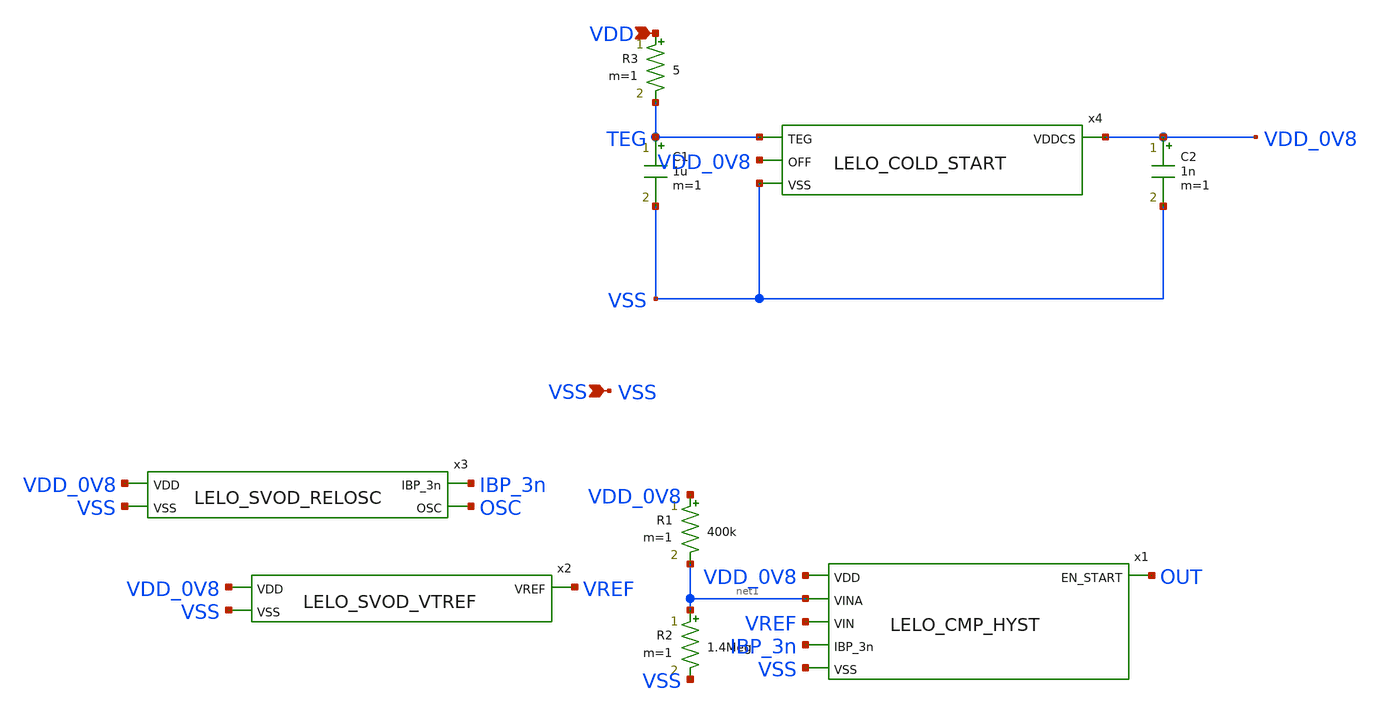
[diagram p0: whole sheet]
** sch_path: design/LELO_SVOD_SKY130A/LELO_STARTUP_DETECTOR_TEST.sch
**.subckt LELO_STARTUP_DETECTOR_TEST VSS VDD
*.ipin VSS
*.ipin VDD
x1 VDD_0V8 OUT net1 VREF IBP_3n VSS LELO_CMP_HYST
x2 VDD_0V8 VSS VREF LELO_SVOD_VTREF
R1 VDD_0V8 net1 400k m=1
R2 net1 VSS 1.4Meg m=1
x3 VDD_0V8 VSS IBP_3n OSC LELO_SVOD_RELOSC
x4 TEG VDD_0V8 VDD_0V8 VSS LELO_COLD_START
R3 VDD TEG 5 m=1
C1 TEG VSS 1u m=1
C2 VDD_0V8 VSS 1n m=1
**.ends
.end
